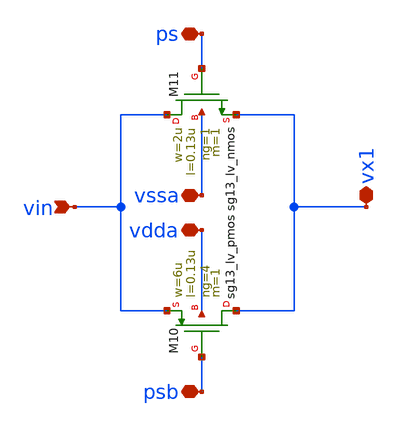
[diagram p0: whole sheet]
** sch_path: 5_Design/4_Layout/Team 5/splitUpSimulationsAndSchematics/integ_5_split2.1.sch
**.subckt integ_5_split2.1 vin psb ps vx1 vdda vssa
*.ipin vin
*.iopin psb
*.iopin ps
*.iopin vx1
*.iopin vdda
*.iopin vssa
XM10 vx1 psb vin vdda sg13_lv_pmos w=6u l=0.13u ng=4 m=1 mm_ok=1
XM11 vin ps vx1 vssa sg13_lv_nmos w=2u l=0.13u ng=1 m=1 mm_ok=1
**.ends
.end
